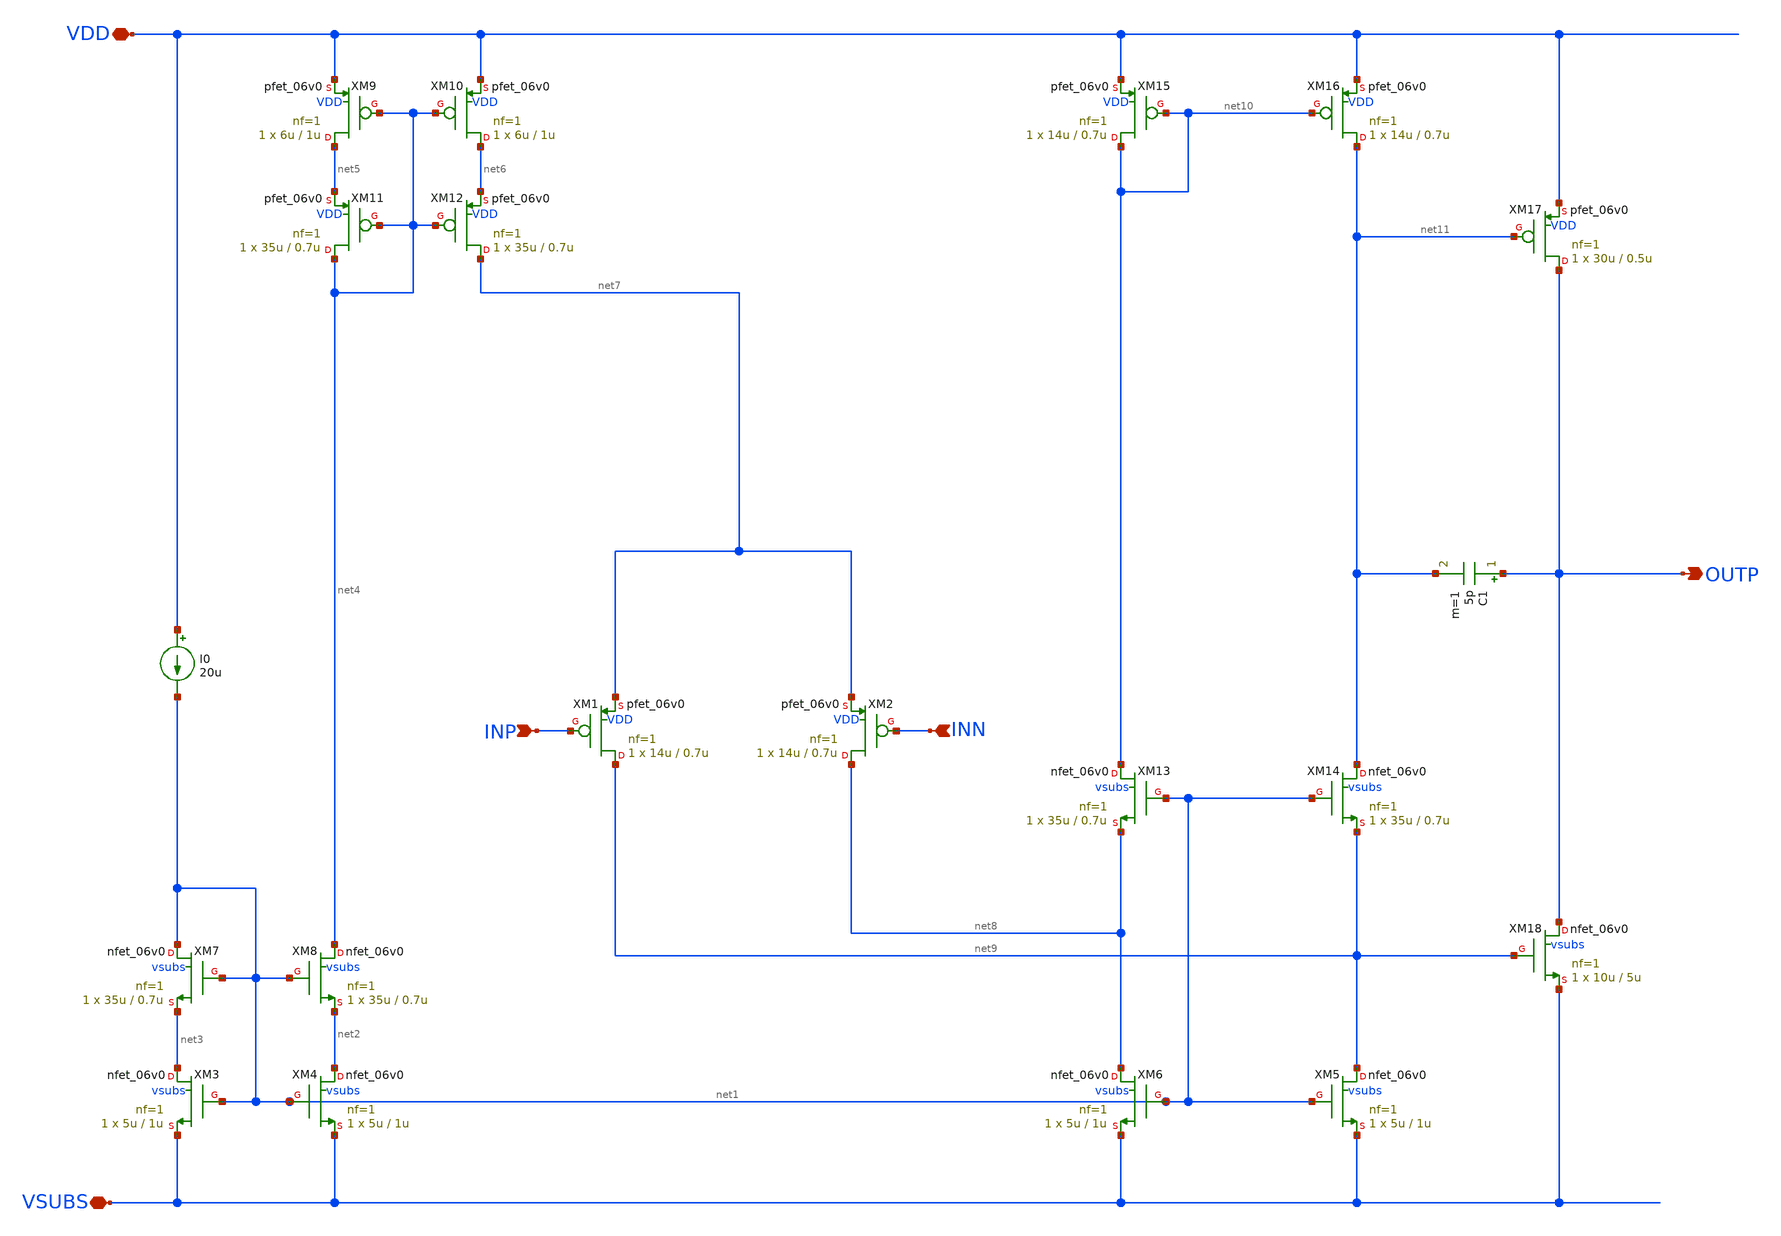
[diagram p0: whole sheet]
** sch_path: xschem/ip_amplifier.sch
**.subckt ip_amplifier VDD VSUBS INP INN OUTP
*.iopin VDD
*.iopin VSUBS
*.ipin INP
*.ipin INN
*.opin OUTP
XM1 net9 INP net7 VDD pfet_06v0 L=0.7u W=14u nf=1 ad='int((nf+1)/2) * W/nf * 0.18u' as='int((nf+2)/2) * W/nf * 0.18u'
+ pd='2*int((nf+1)/2) * (W/nf + 0.18u)' ps='2*int((nf+2)/2) * (W/nf + 0.18u)' nrd='0.18u / W' nrs='0.18u / W'
+ sa=0 sb=0 sd=0 m=1 par=1
XM2 net8 INN net7 VDD pfet_06v0 L=0.7u W=14u nf=1 ad='int((nf+1)/2) * W/nf * 0.18u' as='int((nf+2)/2) * W/nf * 0.18u'
+ pd='2*int((nf+1)/2) * (W/nf + 0.18u)' ps='2*int((nf+2)/2) * (W/nf + 0.18u)' nrd='0.18u / W' nrs='0.18u / W'
+ sa=0 sb=0 sd=0 m=1 par=1
XM5 net9 net1 VSUBS vsubs nfet_06v0 L=1u W=5u nf=1 ad='int((nf+1)/2) * W/nf * 0.18u' as='int((nf+2)/2) * W/nf * 0.18u'
+ pd='2*int((nf+1)/2) * (W/nf + 0.18u)' ps='2*int((nf+2)/2) * (W/nf + 0.18u)' nrd='0.18u / W' nrs='0.18u / W'
+ sa=0 sb=0 sd=0 m=1 par=1
XM6 net8 net1 VSUBS vsubs nfet_06v0 L=1u W=5u nf=1 ad='int((nf+1)/2) * W/nf * 0.18u' as='int((nf+2)/2) * W/nf * 0.18u'
+ pd='2*int((nf+1)/2) * (W/nf + 0.18u)' ps='2*int((nf+2)/2) * (W/nf + 0.18u)' nrd='0.18u / W' nrs='0.18u / W'
+ sa=0 sb=0 sd=0 m=1 par=1
XM3 net3 net1 VSUBS vsubs nfet_06v0 L=1u W=5u nf=1 ad='int((nf+1)/2) * W/nf * 0.18u' as='int((nf+2)/2) * W/nf * 0.18u'
+ pd='2*int((nf+1)/2) * (W/nf + 0.18u)' ps='2*int((nf+2)/2) * (W/nf + 0.18u)' nrd='0.18u / W' nrs='0.18u / W'
+ sa=0 sb=0 sd=0 m=1 par=1
XM4 net2 net1 VSUBS vsubs nfet_06v0 L=1u W=5u nf=1 ad='int((nf+1)/2) * W/nf * 0.18u' as='int((nf+2)/2) * W/nf * 0.18u'
+ pd='2*int((nf+1)/2) * (W/nf + 0.18u)' ps='2*int((nf+2)/2) * (W/nf + 0.18u)' nrd='0.18u / W' nrs='0.18u / W'
+ sa=0 sb=0 sd=0 m=1 par=1
XM7 net1 net1 net3 vsubs nfet_06v0 L=0.7u W=35u nf=1 ad='int((nf+1)/2) * W/nf * 0.18u' as='int((nf+2)/2) * W/nf * 0.18u'
+ pd='2*int((nf+1)/2) * (W/nf + 0.18u)' ps='2*int((nf+2)/2) * (W/nf + 0.18u)' nrd='0.18u / W' nrs='0.18u / W'
+ sa=0 sb=0 sd=0 m=1 par=1
XM8 net4 net1 net2 vsubs nfet_06v0 L=0.7u W=35u nf=1 ad='int((nf+1)/2) * W/nf * 0.18u' as='int((nf+2)/2) * W/nf * 0.18u'
+ pd='2*int((nf+1)/2) * (W/nf + 0.18u)' ps='2*int((nf+2)/2) * (W/nf + 0.18u)' nrd='0.18u / W' nrs='0.18u / W'
+ sa=0 sb=0 sd=0 m=1 par=1
I0 VDD net1 20u
XM9 net5 net4 VDD VDD pfet_06v0 L=1u W=6u nf=1 ad='int((nf+1)/2) * W/nf * 0.18u' as='int((nf+2)/2) * W/nf * 0.18u'
+ pd='2*int((nf+1)/2) * (W/nf + 0.18u)' ps='2*int((nf+2)/2) * (W/nf + 0.18u)' nrd='0.18u / W' nrs='0.18u / W'
+ sa=0 sb=0 sd=0 m=1 par=1
XM10 net6 net4 VDD VDD pfet_06v0 L=1u W=6u nf=1 ad='int((nf+1)/2) * W/nf * 0.18u' as='int((nf+2)/2) * W/nf * 0.18u'
+ pd='2*int((nf+1)/2) * (W/nf + 0.18u)' ps='2*int((nf+2)/2) * (W/nf + 0.18u)' nrd='0.18u / W' nrs='0.18u / W'
+ sa=0 sb=0 sd=0 m=1 par=1
XM11 net4 net4 net5 VDD pfet_06v0 L=0.7u W=35u nf=1 ad='int((nf+1)/2) * W/nf * 0.18u' as='int((nf+2)/2) * W/nf * 0.18u'
+ pd='2*int((nf+1)/2) * (W/nf + 0.18u)' ps='2*int((nf+2)/2) * (W/nf + 0.18u)' nrd='0.18u / W' nrs='0.18u / W'
+ sa=0 sb=0 sd=0 m=1 par=1
XM12 net7 net4 net6 VDD pfet_06v0 L=0.7u W=35u nf=1 ad='int((nf+1)/2) * W/nf * 0.18u' as='int((nf+2)/2) * W/nf * 0.18u'
+ pd='2*int((nf+1)/2) * (W/nf + 0.18u)' ps='2*int((nf+2)/2) * (W/nf + 0.18u)' nrd='0.18u / W' nrs='0.18u / W'
+ sa=0 sb=0 sd=0 m=1 par=1
XM13 net10 net1 net8 vsubs nfet_06v0 L=0.7u W=35u nf=1 ad='int((nf+1)/2) * W/nf * 0.18u' as='int((nf+2)/2) * W/nf * 0.18u'
+ pd='2*int((nf+1)/2) * (W/nf + 0.18u)' ps='2*int((nf+2)/2) * (W/nf + 0.18u)' nrd='0.18u / W' nrs='0.18u / W'
+ sa=0 sb=0 sd=0 m=1 par=1
XM14 net11 net1 net9 vsubs nfet_06v0 L=0.7u W=35u nf=1 ad='int((nf+1)/2) * W/nf * 0.18u' as='int((nf+2)/2) * W/nf * 0.18u'
+ pd='2*int((nf+1)/2) * (W/nf + 0.18u)' ps='2*int((nf+2)/2) * (W/nf + 0.18u)' nrd='0.18u / W' nrs='0.18u / W'
+ sa=0 sb=0 sd=0 m=1 par=1
XM15 net10 net10 VDD VDD pfet_06v0 L=0.7u W=14u nf=1 ad='int((nf+1)/2) * W/nf * 0.18u' as='int((nf+2)/2) * W/nf * 0.18u'
+ pd='2*int((nf+1)/2) * (W/nf + 0.18u)' ps='2*int((nf+2)/2) * (W/nf + 0.18u)' nrd='0.18u / W' nrs='0.18u / W'
+ sa=0 sb=0 sd=0 m=1 par=1
XM16 net11 net10 VDD VDD pfet_06v0 L=0.7u W=14u nf=1 ad='int((nf+1)/2) * W/nf * 0.18u' as='int((nf+2)/2) * W/nf * 0.18u'
+ pd='2*int((nf+1)/2) * (W/nf + 0.18u)' ps='2*int((nf+2)/2) * (W/nf + 0.18u)' nrd='0.18u / W' nrs='0.18u / W'
+ sa=0 sb=0 sd=0 m=1 par=1
XM17 OUTP net11 VDD VDD pfet_06v0 L=0.5u W=30u nf=1 ad='int((nf+1)/2) * W/nf * 0.18u' as='int((nf+2)/2) * W/nf * 0.18u'
+ pd='2*int((nf+1)/2) * (W/nf + 0.18u)' ps='2*int((nf+2)/2) * (W/nf + 0.18u)' nrd='0.18u / W' nrs='0.18u / W'
+ sa=0 sb=0 sd=0 m=1 par=1
XM18 OUTP net9 VSUBS vsubs nfet_06v0 L=5u W=10u nf=1 ad='int((nf+1)/2) * W/nf * 0.18u' as='int((nf+2)/2) * W/nf * 0.18u'
+ pd='2*int((nf+1)/2) * (W/nf + 0.18u)' ps='2*int((nf+2)/2) * (W/nf + 0.18u)' nrd='0.18u / W' nrs='0.18u / W'
+ sa=0 sb=0 sd=0 m=1 par=1
C1 OUTP net11 5p m=1
**.ends
.end
